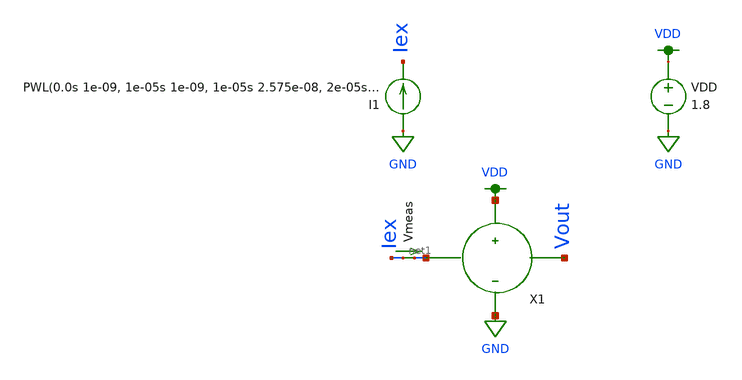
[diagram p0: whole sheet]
** sch_path: schematic/tran_besrour_neuron.sch
**.subckt tran_besrour_neuron
VDD VDD GND 1.8
I1 GND Iex PWL(0.0s 1e-09, 1e-05s 1e-09, 1e-05s 2.575e-08, 2e-05s 2.575e-08, 2e-05s 5.05e-08, 3e-05s
+ 5.05e-08, 3e-05s 7.525e-08, 4e-05s 7.525e-08, 4e-05s 1e-07, 5e-05s 1e-07, 5e-05s 1.9e-07, 6e-05s 1.9e-07,
+ 6e-05s 2.8e-07, 7e-05s 2.8e-07, 7e-05s 3.7e-07, 8e-05s 3.7e-07, 8e-05s 4.6e-07, 9e-05s 4.6e-07, 9e-05s
+ 5.5e-07, 0.0001s 5.5e-07, 0.0001s 6.4e-07, 0.00011s 6.4e-07, 0.00011s 7.3e-07, 0.00012s 7.3e-07, 0.00012s
+ 8.2e-07, 0.00013s 8.2e-07, 0.00013s 9.1e-07, 0.00014s 9.1e-07, 0.00014s 1e-06, 0.00015s 1e-06, 0.00015s
+ 2.8e-06, 0.00016s 2.8e-06, 0.00016s 4.6e-06, 0.00017s 4.6e-06, 0.00017s 6.4e-06, 0.00018s 6.4e-06, 0.00018s
+ 8.2e-06, 0.00019s 8.2e-06, 0.00019s 1e-05, 0.0002s 1e-05, 0.0002s 2.267e-05, 0.00021s 2.267e-05, 0.00021s
+ 3.533e-05, 0.00022s 3.533e-05, 0.00022s 4.8e-05, 0.00023s 4.8e-05, 0.00023s 6.067e-05, 0.00024s 6.067e-05,
+ 0.00024s 7.333e-05, 0.00025s 7.333e-05, 0.00025s 8.6e-05, 0.00026s 8.6e-05, 0.00026s 9.867e-05, 0.00027s
+ 9.867e-05, 0.00027s 0.000111333, 0.00028s 0.000111333, 0.00028s 0.000124, 0.00029s 0.000124, 0.00029s
+ 0.000136667, 0.0003s 0.000136667, 0.0003s 0.000149333, 0.00031s 0.000149333, 0.00031s 0.000162, 0.00032s
+ 0.000162, 0.00032s 0.000174667, 0.00033s 0.000174667, 0.00033s 0.000187333, 0.00034s 0.000187333, 0.00034s
+ 0.0002, 0.00035s 0.0002)
Vmeas Iex net1 0
.save i(vmeas)
X1 net1 Vout VDD GND neuron_top
**** begin user architecture code

.param W=2
.param L=0.3
.include ~/neuromorphic_computing_final/schematic/neuron_top.spice
.control
set wr_vecnames
set wr_singlescale
save all
tran 1ns 350us
wrdata ~/neuromorphic_computing_final/simulation/besrour/mem.txt i(Vmeas) v(Vout)
set appendwrite
.endc



.option wnflag=1
.param MC_SWITCH=0.0
.lib ~/skywater/skywater-pdk/libraries/sky130_fd_pr_ngspice/latest/models/sky130.lib.spice tt

**** end user architecture code
**.ends
.GLOBAL GND
.GLOBAL VDD
.end
